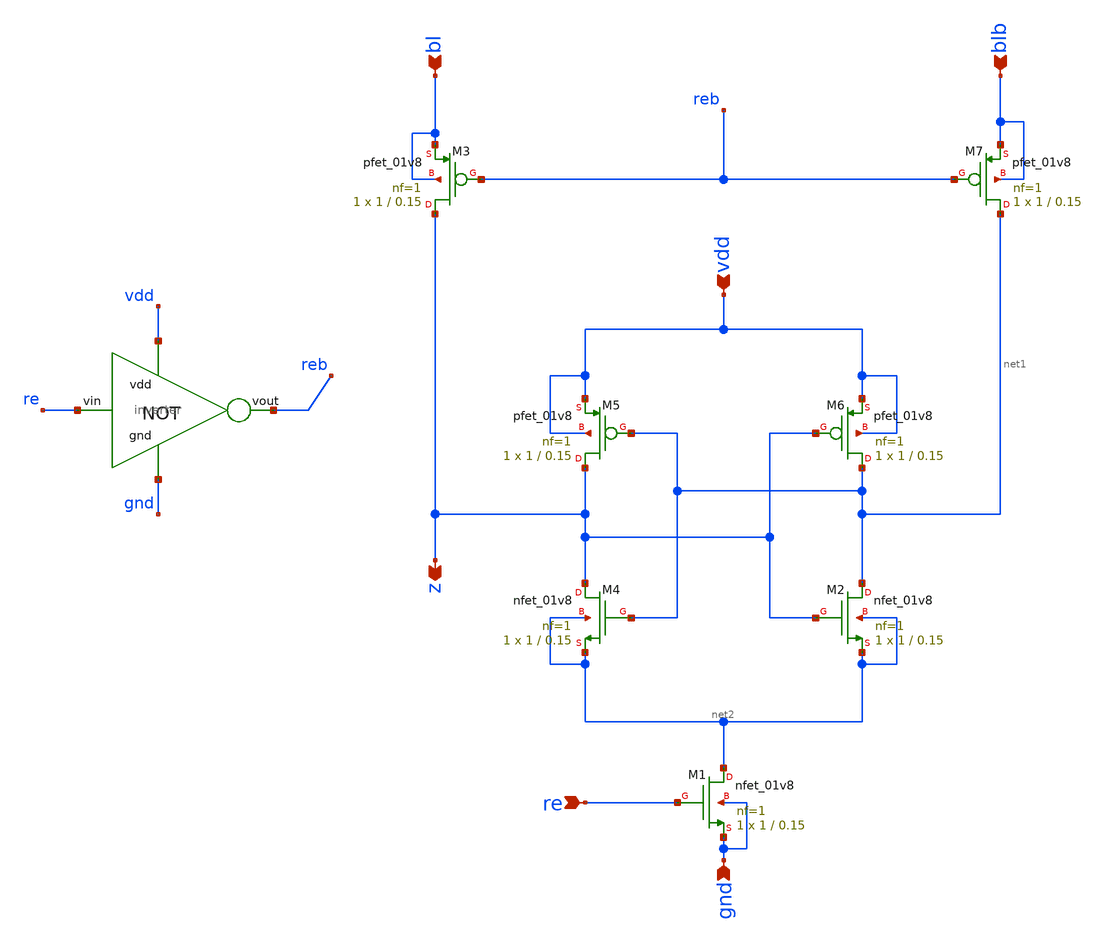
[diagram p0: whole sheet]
** sch_path: sram/sense_amp.sch
**.subckt sense_amp gnd vdd z bl blb re
*.ipin gnd
*.ipin vdd
*.opin z
*.ipin bl
*.ipin blb
*.ipin re
XM5 z net1 vdd vdd sky130_fd_pr__pfet_01v8 L=0.15 W=1 nf=1 ad='int((nf+1)/2) * W/nf * 0.29' as='int((nf+2)/2) * W/nf * 0.29'
+ pd='2*int((nf+1)/2) * (W/nf + 0.29)' ps='2*int((nf+2)/2) * (W/nf + 0.29)' nrd='0.29 / W' nrs='0.29 / W'
+ sa=0 sb=0 sd=0 mult=1 m=1
XM6 net1 z vdd vdd sky130_fd_pr__pfet_01v8 L=0.15 W=1 nf=1 ad='int((nf+1)/2) * W/nf * 0.29' as='int((nf+2)/2) * W/nf * 0.29'
+ pd='2*int((nf+1)/2) * (W/nf + 0.29)' ps='2*int((nf+2)/2) * (W/nf + 0.29)' nrd='0.29 / W' nrs='0.29 / W'
+ sa=0 sb=0 sd=0 mult=1 m=1
XM2 net1 z net2 net2 sky130_fd_pr__nfet_01v8 L=0.15 W=1 nf=1 ad='int((nf+1)/2) * W/nf * 0.29' as='int((nf+2)/2) * W/nf * 0.29'
+ pd='2*int((nf+1)/2) * (W/nf + 0.29)' ps='2*int((nf+2)/2) * (W/nf + 0.29)' nrd='0.29 / W' nrs='0.29 / W'
+ sa=0 sb=0 sd=0 mult=1 m=1
XM4 z net1 net2 net2 sky130_fd_pr__nfet_01v8 L=0.15 W=1 nf=1 ad='int((nf+1)/2) * W/nf * 0.29' as='int((nf+2)/2) * W/nf * 0.29'
+ pd='2*int((nf+1)/2) * (W/nf + 0.29)' ps='2*int((nf+2)/2) * (W/nf + 0.29)' nrd='0.29 / W' nrs='0.29 / W'
+ sa=0 sb=0 sd=0 mult=1 m=1
XM1 net2 re gnd gnd sky130_fd_pr__nfet_01v8 L=0.15 W=1 nf=1 ad='int((nf+1)/2) * W/nf * 0.29' as='int((nf+2)/2) * W/nf * 0.29'
+ pd='2*int((nf+1)/2) * (W/nf + 0.29)' ps='2*int((nf+2)/2) * (W/nf + 0.29)' nrd='0.29 / W' nrs='0.29 / W'
+ sa=0 sb=0 sd=0 mult=1 m=1
XM3 z reb bl bl sky130_fd_pr__pfet_01v8 L=0.15 W=1 nf=1 ad='int((nf+1)/2) * W/nf * 0.29' as='int((nf+2)/2) * W/nf * 0.29'
+ pd='2*int((nf+1)/2) * (W/nf + 0.29)' ps='2*int((nf+2)/2) * (W/nf + 0.29)' nrd='0.29 / W' nrs='0.29 / W'
+ sa=0 sb=0 sd=0 mult=1 m=1
XM7 net1 reb blb blb sky130_fd_pr__pfet_01v8 L=0.15 W=1 nf=1 ad='int((nf+1)/2) * W/nf * 0.29' as='int((nf+2)/2) * W/nf * 0.29'
+ pd='2*int((nf+1)/2) * (W/nf + 0.29)' ps='2*int((nf+2)/2) * (W/nf + 0.29)' nrd='0.29 / W' nrs='0.29 / W'
+ sa=0 sb=0 sd=0 mult=1 m=1
x1 vdd re reb gnd inverter
**.ends

* expanding   symbol:  inverter.sym # of pins=4
** sym_path: sram/inverter.sym
** sch_path: sram/inverter.sch
.subckt inverter vdd vin vout gnd
*.ipin vin
*.ipin vdd
*.ipin gnd
*.opin vout
XM1 vout vin gnd gnd sky130_fd_pr__nfet_01v8 L=0.15 W=1 nf=1 ad='int((nf+1)/2) * W/nf * 0.29' as='int((nf+2)/2) * W/nf * 0.29'
+ pd='2*int((nf+1)/2) * (W/nf + 0.29)' ps='2*int((nf+2)/2) * (W/nf + 0.29)' nrd='0.29 / W' nrs='0.29 / W'
+ sa=0 sb=0 sd=0 mult=1 m=1
XM2 vout vin vdd vdd sky130_fd_pr__pfet_01v8 L=0.15 W=1 nf=1 ad='int((nf+1)/2) * W/nf * 0.29' as='int((nf+2)/2) * W/nf * 0.29'
+ pd='2*int((nf+1)/2) * (W/nf + 0.29)' ps='2*int((nf+2)/2) * (W/nf + 0.29)' nrd='0.29 / W' nrs='0.29 / W'
+ sa=0 sb=0 sd=0 mult=1 m=1
.ends

.end
